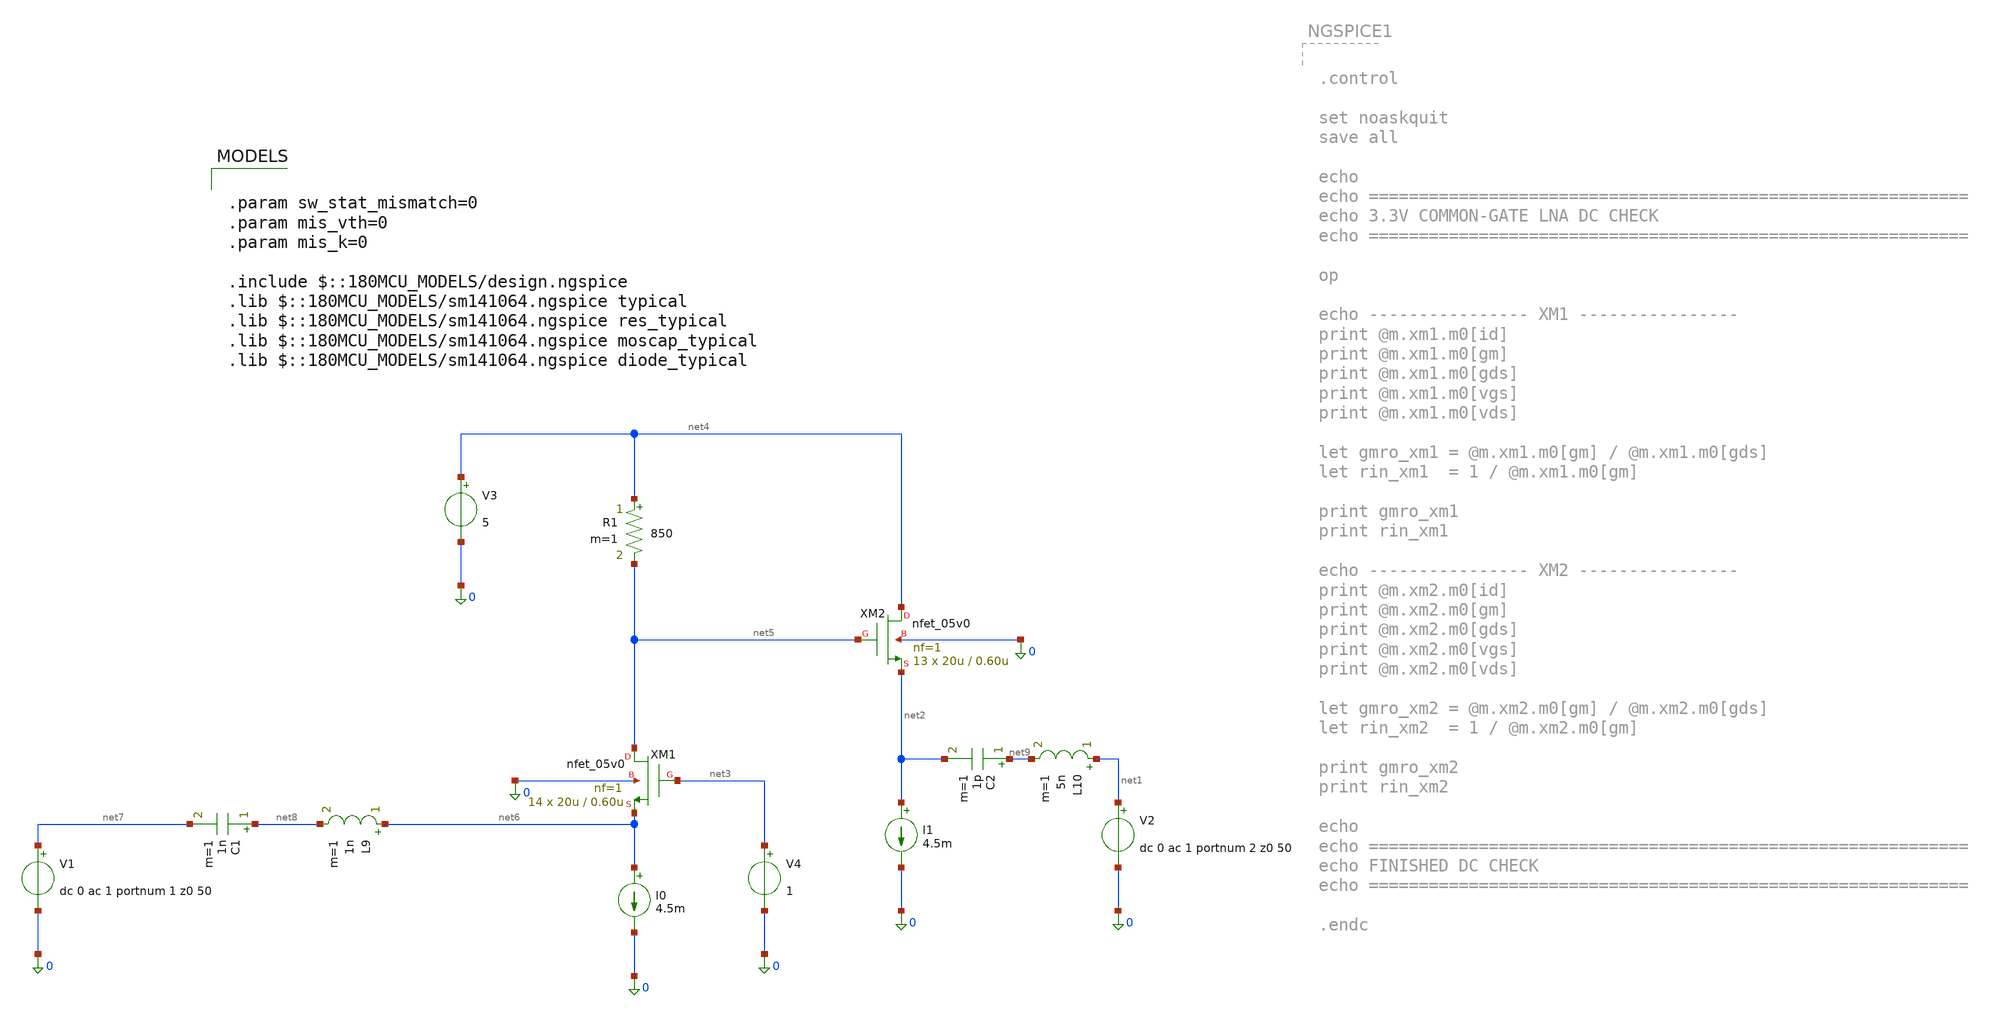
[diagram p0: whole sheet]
** sch_path: LNA_gain_test/test_5v.sch
**.subckt test_5v
I0 net6 0 4.5m
C1 net8 net7 1n m=1
C2 net9 net2 1p m=1
I1 net2 0 4.5m
V1 net7 0 dc 0 ac 1 portnum 1 z0 50
V2 net1 0 dc 0 ac 1 portnum 2 z0 50
R1 net4 net5 850 m=1
V3 net4 0 5
V4 net3 0 1
L9 net6 net8 1n m=1
L10 net1 net9 5n m=1
XM2 net4 net5 net2 0 nfet_05v0 L=0.60u W=20u nf=1 ad='int((nf+1)/2) * W/nf * 0.18u' as='int((nf+2)/2) * W/nf * 0.18u'
+ pd='2*int((nf+1)/2) * (W/nf + 0.18u)' ps='2*int((nf+2)/2) * (W/nf + 0.18u)' nrd='0.18u / W' nrs='0.18u / W'
+ sa=0 sb=0 sd=0 m=13
XM1 net5 net3 net6 0 nfet_05v0 L=0.60u W=20u nf=1 ad='int((nf+1)/2) * W/nf * 0.18u' as='int((nf+2)/2) * W/nf * 0.18u'
+ pd='2*int((nf+1)/2) * (W/nf + 0.18u)' ps='2*int((nf+2)/2) * (W/nf + 0.18u)' nrd='0.18u / W' nrs='0.18u / W'
+ sa=0 sb=0 sd=0 m=14
**** begin user architecture code

.param sw_stat_mismatch=0
.param mis_vth=0
.param mis_k=0

.include $::180MCU_MODELS/design.ngspice
.lib $::180MCU_MODELS/sm141064.ngspice typical
.lib $::180MCU_MODELS/sm141064.ngspice res_typical
.lib $::180MCU_MODELS/sm141064.ngspice moscap_typical
.lib $::180MCU_MODELS/sm141064.ngspice diode_typical



.control

set noaskquit
set wr_singlescale
set wr_vecnames
save all

echo
echo ============================================================
echo 5V COMMON-GATE LNA CHECK
echo Device target: nfet_06v0
echo Target frequency: 2.4 GHz
echo Target gm for 50 ohm CG input: 20 mS
echo ============================================================

op

echo
echo ---------------- XM1 DC CHECK ----------------
print @m.xm1.m0[id]
print @m.xm1.m0[gm]
print @m.xm1.m0[gds]
print @m.xm1.m0[vgs]
print @m.xm1.m0[vds]
print @m.xm1.m0[vth]
print @m.xm1.m0[vdsat]

let gmro_xm1 = @m.xm1.m0[gm] / @m.xm1.m0[gds]
let ro_xm1   = 1 / @m.xm1.m0[gds]
let rin_xm1  = 1 / @m.xm1.m0[gm]

print gmro_xm1
print ro_xm1
print rin_xm1

echo
echo ---------------- XM2 DC CHECK ----------------
print @m.xm2.m0[id]
print @m.xm2.m0[gm]
print @m.xm2.m0[gds]
print @m.xm2.m0[vgs]
print @m.xm2.m0[vds]
print @m.xm2.m0[vth]
print @m.xm2.m0[vdsat]

let gmro_xm2 = @m.xm2.m0[gm] / @m.xm2.m0[gds]
let ro_xm2   = 1 / @m.xm2.m0[gds]
let rin_xm2  = 1 / @m.xm2.m0[gm]

print gmro_xm2
print ro_xm2
print rin_xm2

echo
echo ============================================================
echo RUNNING S-PARAMETER SWEEP
echo ============================================================

sp dec 401 100Meg 6G

let s11_db = db(sp1.s_1_1)
let s21_db = db(sp1.s_2_1)
let s12_db = db(sp1.s_1_2)
let s22_db = db(sp1.s_2_2)

let s11_mag = mag(sp1.s_1_1)
let s21_mag = mag(sp1.s_2_1)
let s22_mag = mag(sp1.s_2_2)

let z0 = 50

let zin = z0 * (1 + sp1.s_1_1) / (1 - sp1.s_1_1)
let zin_re = real(zin)
let zin_im = imag(zin)
let zin_mag = mag(zin)

let zout = z0 * (1 + sp1.s_2_2) / (1 - sp1.s_2_2)
let zout_re = real(zout)
let zout_im = imag(zout)
let zout_mag = mag(zout)

echo
echo ============================================================
echo EXACT 5V RESULTS AT 2.4 GHz
echo ============================================================

meas sp s11_2p4g find s11_db at=2.4G
meas sp s21_2p4g find s21_db at=2.4G
meas sp s12_2p4g find s12_db at=2.4G
meas sp s22_2p4g find s22_db at=2.4G

meas sp s11_mag_2p4g find s11_mag at=2.4G
meas sp s21_mag_2p4g find s21_mag at=2.4G
meas sp s22_mag_2p4g find s22_mag at=2.4G

meas sp zin_re_2p4g find zin_re at=2.4G
meas sp zin_im_2p4g find zin_im at=2.4G
meas sp zin_mag_2p4g find zin_mag at=2.4G

meas sp zout_re_2p4g find zout_re at=2.4G
meas sp zout_im_2p4g find zout_im at=2.4G
meas sp zout_mag_2p4g find zout_mag at=2.4G

echo
echo ============================================================
echo CHECKPOINT GAIN VALUES
echo ============================================================

meas sp s21_500m find s21_db at=500Meg
meas sp s21_1g find s21_db at=1G
meas sp s21_1p5g find s21_db at=1.5G
meas sp s21_2g find s21_db at=2G
meas sp s21_2p4g_check find s21_db at=2.4G
meas sp s21_3g find s21_db at=3G
meas sp s21_4g find s21_db at=4G
meas sp s21_5g find s21_db at=5G

echo
echo ============================================================
echo WRITING CSV FILE
echo ============================================================

wrdata lna_5v_2p4g_check.csv frequency s11_db s21_db s12_db s22_db s11_mag s21_mag s22_mag zin_re
+ zin_im zin_mag zout_re zout_im zout_mag

echo
echo ============================================================
echo 5V CHECK COMPLETE
echo Wrote file:
echo lna_5v_2p4g_check.csv
echo ============================================================

.endc


**** end user architecture code
**.ends
.end
